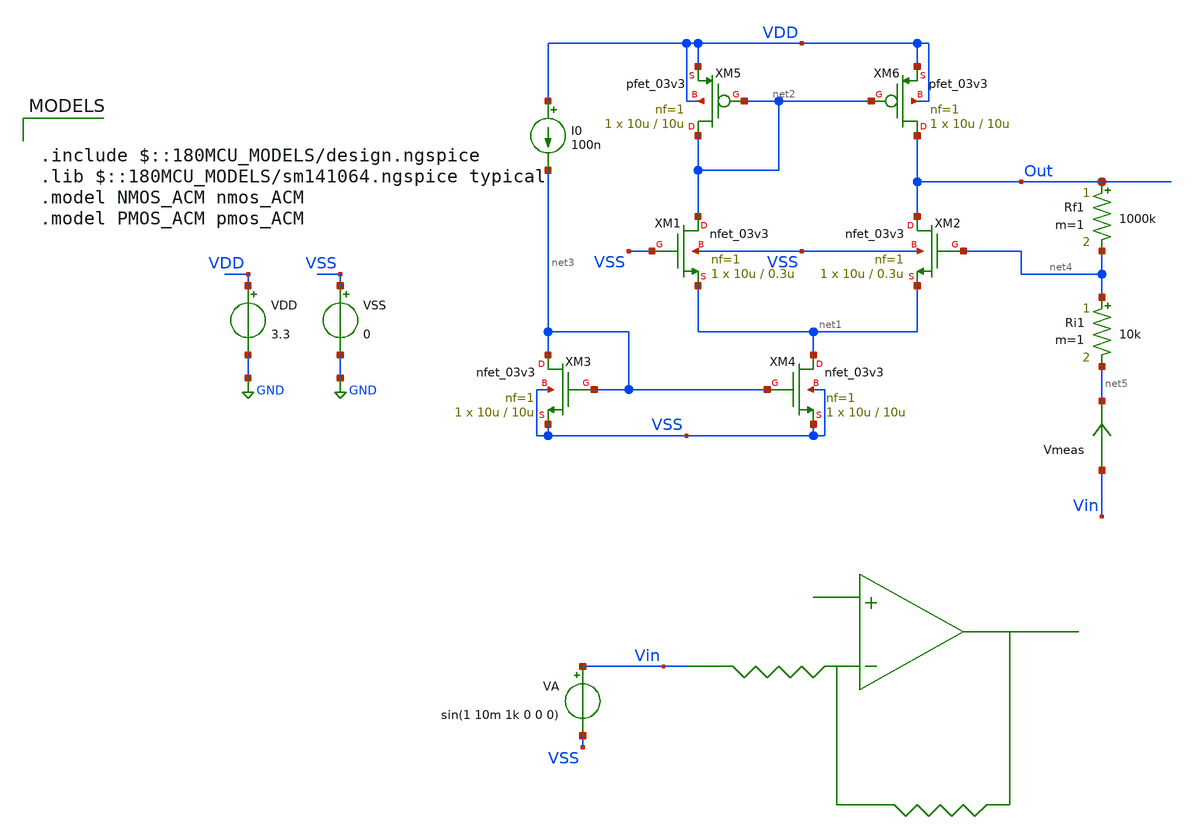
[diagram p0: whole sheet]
** sch_path: Examples/GF180MCU/xschem/TB_ampDiff_acm.sch
**.subckt TB_ampDiff_acm
VDD VDD GND 3.3
VSS VSS GND 0
I0 VDD net3 100n
VA Vin VSS sin(1 10m 1k 0 0 0)
Rf1 Out net4 1000k m=1
Ri1 net4 net5 10k m=1
XM1 net2 VSS net1 VSS nfet_03v3 L=0.3u W=10u nf=1 ad='int((nf+1)/2) * W/nf * 0.18u' as='int((nf+2)/2) * W/nf * 0.18u'
+ pd='2*int((nf+1)/2) * (W/nf + 0.18u)' ps='2*int((nf+2)/2) * (W/nf + 0.18u)' nrd='0.18u / W' nrs='0.18u / W'
+ sa=0 sb=0 sd=0 m=1
XM2 Out net4 net1 VSS nfet_03v3 L=0.3u W=10u nf=1 ad='int((nf+1)/2) * W/nf * 0.18u' as='int((nf+2)/2) * W/nf * 0.18u'
+ pd='2*int((nf+1)/2) * (W/nf + 0.18u)' ps='2*int((nf+2)/2) * (W/nf + 0.18u)' nrd='0.18u / W' nrs='0.18u / W'
+ sa=0 sb=0 sd=0 m=1
XM3 net3 net3 VSS VSS nfet_03v3 L=10u W=10u nf=1 ad='int((nf+1)/2) * W/nf * 0.18u' as='int((nf+2)/2) * W/nf * 0.18u'
+ pd='2*int((nf+1)/2) * (W/nf + 0.18u)' ps='2*int((nf+2)/2) * (W/nf + 0.18u)' nrd='0.18u / W' nrs='0.18u / W'
+ sa=0 sb=0 sd=0 m=1
XM4 net1 net3 VSS VSS nfet_03v3 L=10u W=10u nf=1 ad='int((nf+1)/2) * W/nf * 0.18u' as='int((nf+2)/2) * W/nf * 0.18u'
+ pd='2*int((nf+1)/2) * (W/nf + 0.18u)' ps='2*int((nf+2)/2) * (W/nf + 0.18u)' nrd='0.18u / W' nrs='0.18u / W'
+ sa=0 sb=0 sd=0 m=1
XM5 net2 net2 VDD VDD pfet_03v3 L=10u W=10u nf=1 ad='int((nf+1)/2) * W/nf * 0.18u' as='int((nf+2)/2) * W/nf * 0.18u'
+ pd='2*int((nf+1)/2) * (W/nf + 0.18u)' ps='2*int((nf+2)/2) * (W/nf + 0.18u)' nrd='0.18u / W' nrs='0.18u / W'
+ sa=0 sb=0 sd=0 m=1
XM6 Out net2 VDD VDD pfet_03v3 L=10u W=10u nf=1 ad='int((nf+1)/2) * W/nf * 0.18u' as='int((nf+2)/2) * W/nf * 0.18u'
+ pd='2*int((nf+1)/2) * (W/nf + 0.18u)' ps='2*int((nf+2)/2) * (W/nf + 0.18u)' nrd='0.18u / W' nrs='0.18u / W'
+ sa=0 sb=0 sd=0 m=1
Vmeas Vin net5 0
.save i(vmeas)
**** begin user architecture code

.include $::180MCU_MODELS/design.ngspice
.lib $::180MCU_MODELS/sm141064.ngspice typical
.model NMOS_ACM nmos_ACM
.model PMOS_ACM pmos_ACM



.option gmin=1e-15
.control
pre_osdi /home/gmaranhao/Documents/MOSFET_model/Examples/GF180MCU/xschem/symbol/NMOS_ACM_2V0.osdi
pre_osdi /home/gmaranhao/Documents/MOSFET_model/Examples/GF180MCU/xschem/symbol/PMOS_ACM_2V0.osdi
save all


tran 1u 1m
remzerovec
write TB_ampDiff_acm.raw
set appendwrite

.endc


**** end user architecture code
**.ends
.GLOBAL GND
.end
